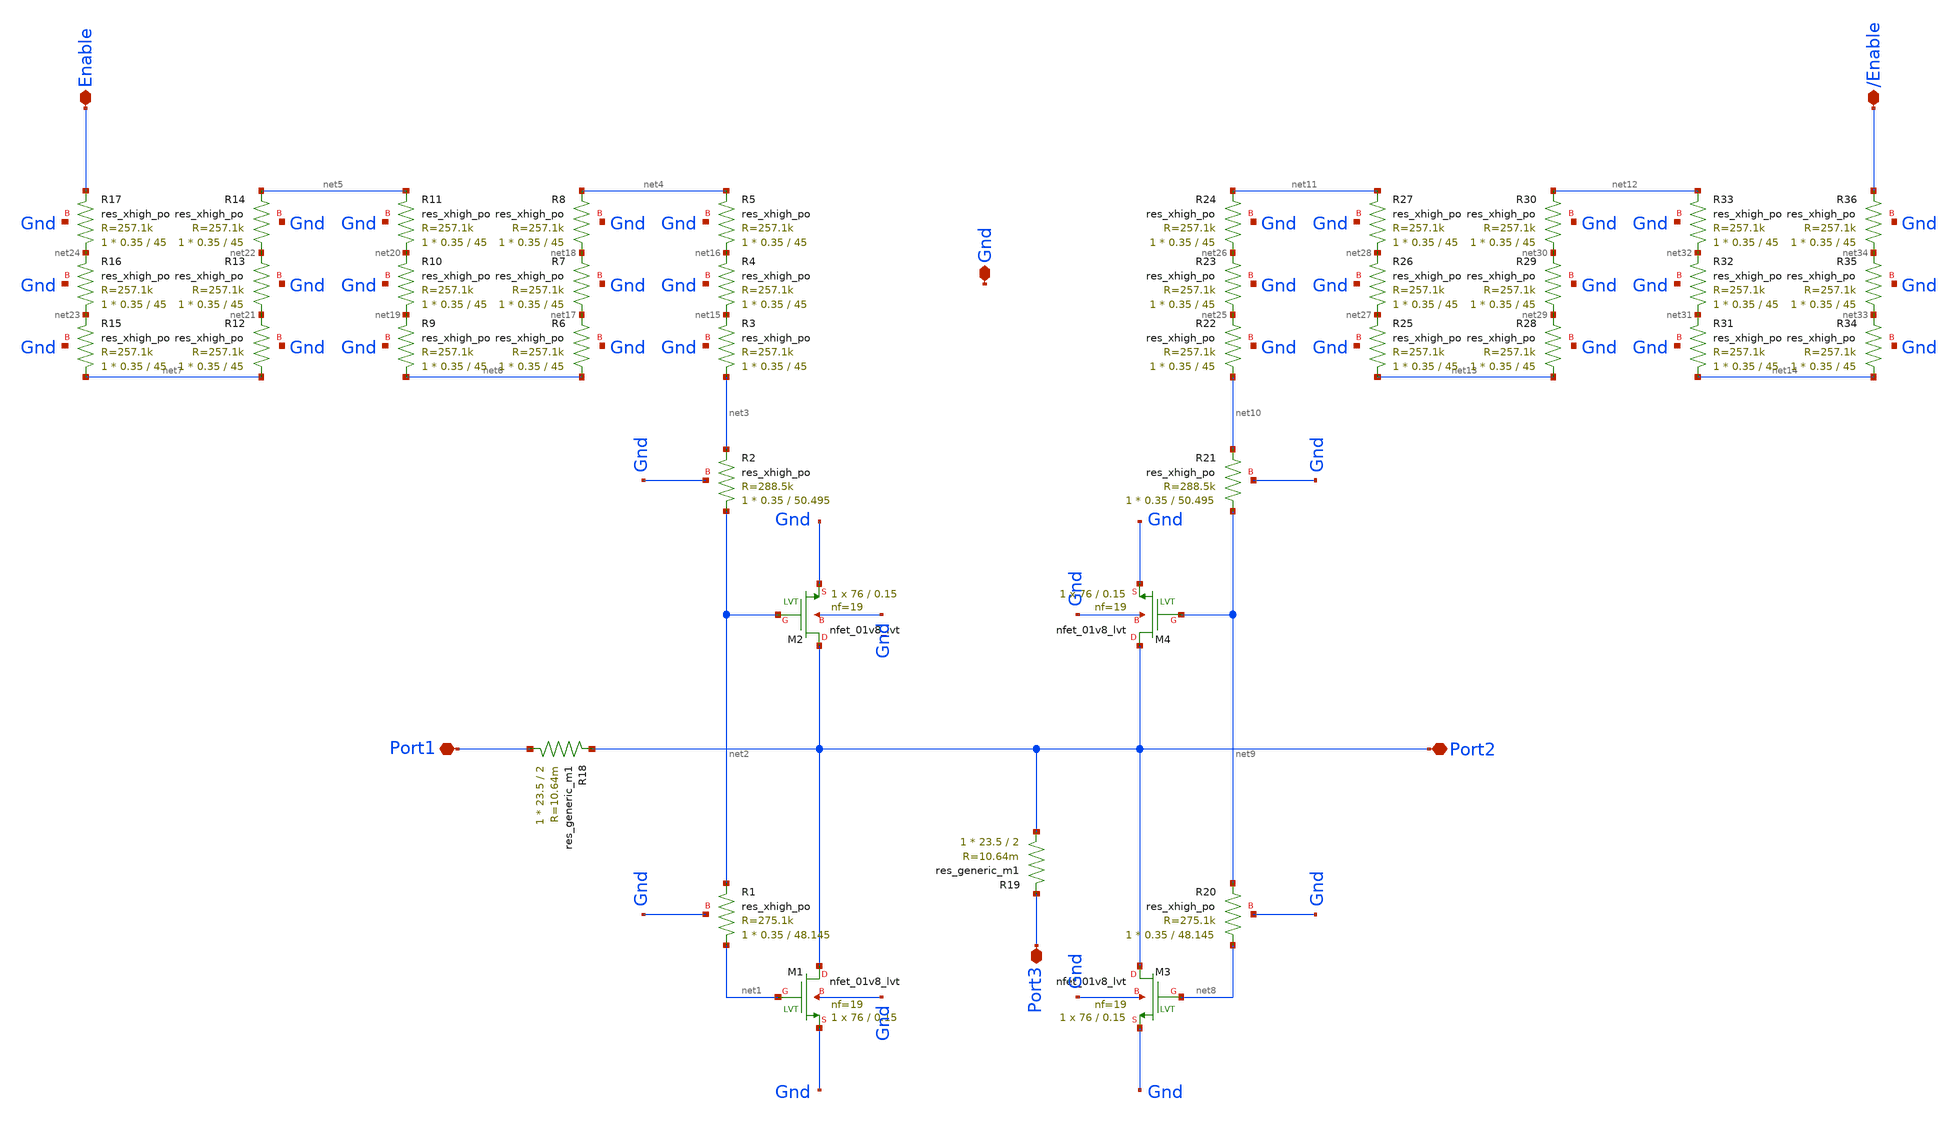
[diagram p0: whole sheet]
** sch_path: Switch_tapeout/xschem/switch_terminals.sch
**.subckt switch_terminals Port1 Port2 Port3 Enable /Enable Gnd
*.iopin Port1
*.iopin Port2
*.iopin Port3
*.iopin Enable
*.iopin /Enable
*.iopin Gnd
XM1 Port2 net1 Gnd Gnd sky130_fd_pr__nfet_01v8_lvt L=0.15 W=76 nf=19 ad='int((nf+1)/2) * W/nf * 0.29'
+ as='int((nf+2)/2) * W/nf * 0.29' pd='2*int((nf+1)/2) * (W/nf + 0.29)' ps='2*int((nf+2)/2) * (W/nf + 0.29)'
+ nrd='0.29 / W' nrs='0.29 / W' sa=0 sb=0 sd=0 mult=1 m=1
XR1 net1 net2 Gnd sky130_fd_pr__res_xhigh_po W=0.35 L=48.145 mult=1 m=1
XM2 Port2 net2 Gnd Gnd sky130_fd_pr__nfet_01v8_lvt L=0.15 W=76 nf=19 ad='int((nf+1)/2) * W/nf * 0.29'
+ as='int((nf+2)/2) * W/nf * 0.29' pd='2*int((nf+1)/2) * (W/nf + 0.29)' ps='2*int((nf+2)/2) * (W/nf + 0.29)'
+ nrd='0.29 / W' nrs='0.29 / W' sa=0 sb=0 sd=0 mult=1 m=1
XR2 net2 net3 Gnd sky130_fd_pr__res_xhigh_po W=0.35 L=50.495 mult=1 m=1
XR3 net3 net15 Gnd sky130_fd_pr__res_xhigh_po W=0.35 L=45 mult=1 m=1
XR4 net15 net16 Gnd sky130_fd_pr__res_xhigh_po W=0.35 L=45 mult=1 m=1
XR5 net16 net4 Gnd sky130_fd_pr__res_xhigh_po W=0.35 L=45 mult=1 m=1
XR6 net6 net17 Gnd sky130_fd_pr__res_xhigh_po W=0.35 L=45 mult=1 m=1
XR7 net17 net18 Gnd sky130_fd_pr__res_xhigh_po W=0.35 L=45 mult=1 m=1
XR8 net18 net4 Gnd sky130_fd_pr__res_xhigh_po W=0.35 L=45 mult=1 m=1
XR9 net6 net19 Gnd sky130_fd_pr__res_xhigh_po W=0.35 L=45 mult=1 m=1
XR10 net19 net20 Gnd sky130_fd_pr__res_xhigh_po W=0.35 L=45 mult=1 m=1
XR11 net20 net5 Gnd sky130_fd_pr__res_xhigh_po W=0.35 L=45 mult=1 m=1
XR12 net7 net21 Gnd sky130_fd_pr__res_xhigh_po W=0.35 L=45 mult=1 m=1
XR13 net21 net22 Gnd sky130_fd_pr__res_xhigh_po W=0.35 L=45 mult=1 m=1
XR14 net22 net5 Gnd sky130_fd_pr__res_xhigh_po W=0.35 L=45 mult=1 m=1
XR15 net7 net23 Gnd sky130_fd_pr__res_xhigh_po W=0.35 L=45 mult=1 m=1
XR16 net23 net24 Gnd sky130_fd_pr__res_xhigh_po W=0.35 L=45 mult=1 m=1
XR17 net24 Enable Gnd sky130_fd_pr__res_xhigh_po W=0.35 L=45 mult=1 m=1
R18 Port1 Port2 sky130_fd_pr__res_generic_m1 W=23.5 L=2 m=1
R19 Port2 Port3 sky130_fd_pr__res_generic_m1 W=23.5 L=2 m=1
XM3 Port2 net8 Gnd Gnd sky130_fd_pr__nfet_01v8_lvt L=0.15 W=76 nf=19 ad='int((nf+1)/2) * W/nf * 0.29'
+ as='int((nf+2)/2) * W/nf * 0.29' pd='2*int((nf+1)/2) * (W/nf + 0.29)' ps='2*int((nf+2)/2) * (W/nf + 0.29)'
+ nrd='0.29 / W' nrs='0.29 / W' sa=0 sb=0 sd=0 mult=1 m=1
XR20 net8 net9 Gnd sky130_fd_pr__res_xhigh_po W=0.35 L=48.145 mult=1 m=1
XM4 Port2 net9 Gnd Gnd sky130_fd_pr__nfet_01v8_lvt L=0.15 W=76 nf=19 ad='int((nf+1)/2) * W/nf * 0.29'
+ as='int((nf+2)/2) * W/nf * 0.29' pd='2*int((nf+1)/2) * (W/nf + 0.29)' ps='2*int((nf+2)/2) * (W/nf + 0.29)'
+ nrd='0.29 / W' nrs='0.29 / W' sa=0 sb=0 sd=0 mult=1 m=1
XR21 net9 net10 Gnd sky130_fd_pr__res_xhigh_po W=0.35 L=50.495 mult=1 m=1
XR22 net10 net25 Gnd sky130_fd_pr__res_xhigh_po W=0.35 L=45 mult=1 m=1
XR23 net25 net26 Gnd sky130_fd_pr__res_xhigh_po W=0.35 L=45 mult=1 m=1
XR24 net26 net11 Gnd sky130_fd_pr__res_xhigh_po W=0.35 L=45 mult=1 m=1
XR25 net13 net27 Gnd sky130_fd_pr__res_xhigh_po W=0.35 L=45 mult=1 m=1
XR26 net27 net28 Gnd sky130_fd_pr__res_xhigh_po W=0.35 L=45 mult=1 m=1
XR27 net28 net11 Gnd sky130_fd_pr__res_xhigh_po W=0.35 L=45 mult=1 m=1
XR28 net13 net29 Gnd sky130_fd_pr__res_xhigh_po W=0.35 L=45 mult=1 m=1
XR29 net29 net30 Gnd sky130_fd_pr__res_xhigh_po W=0.35 L=45 mult=1 m=1
XR30 net30 net12 Gnd sky130_fd_pr__res_xhigh_po W=0.35 L=45 mult=1 m=1
XR31 net14 net31 Gnd sky130_fd_pr__res_xhigh_po W=0.35 L=45 mult=1 m=1
XR32 net31 net32 Gnd sky130_fd_pr__res_xhigh_po W=0.35 L=45 mult=1 m=1
XR33 net32 net12 Gnd sky130_fd_pr__res_xhigh_po W=0.35 L=45 mult=1 m=1
XR34 net14 net33 Gnd sky130_fd_pr__res_xhigh_po W=0.35 L=45 mult=1 m=1
XR35 net33 net34 Gnd sky130_fd_pr__res_xhigh_po W=0.35 L=45 mult=1 m=1
XR36 net34 /Enable Gnd sky130_fd_pr__res_xhigh_po W=0.35 L=45 mult=1 m=1
**.ends
.end
